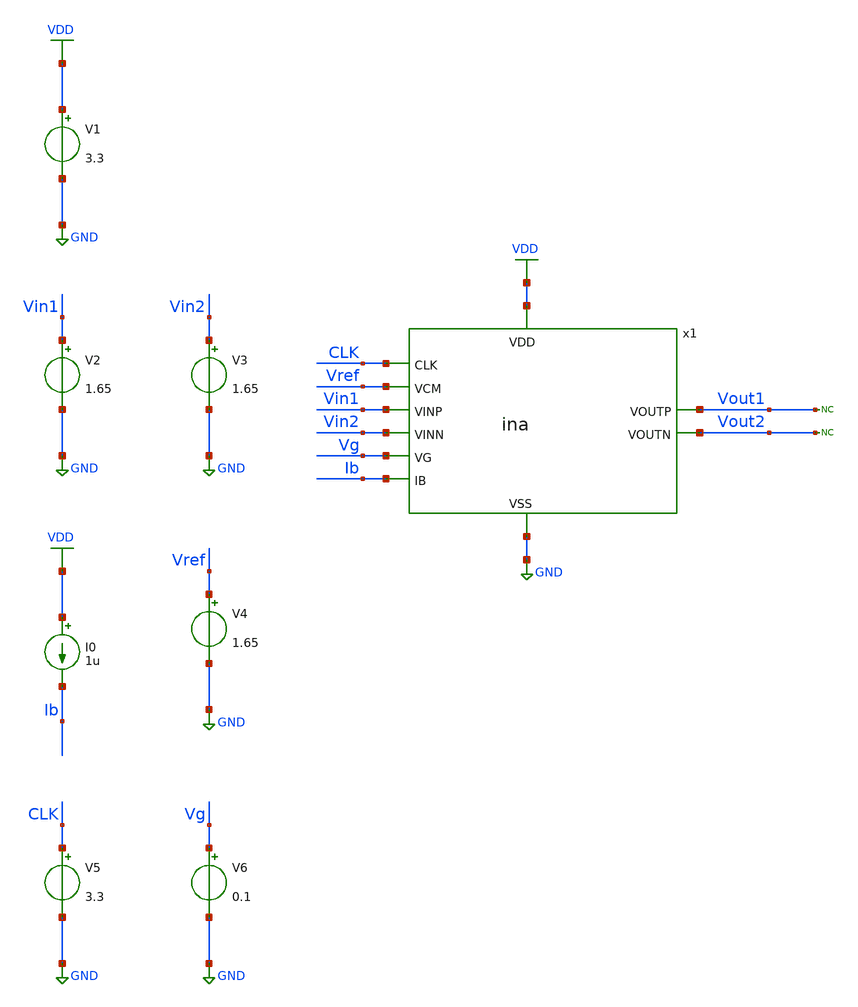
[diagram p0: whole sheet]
** sch_path: designs/libs/tb_ina/tb_ina_op/tb_ina_op.sch
**.subckt tb_ina_op
V1 VDD GND 3.3
V2 Vin1 GND 1.65
V3 Vin2 GND 1.65
V4 Vref GND 1.65
x1 Vg VDD Vin1 Vin2 CLK Vout1 Vout2 GND Vref Ib ina
V5 CLK GND 3.3
V6 Vg GND 0.1
I0 VDD Ib 1u
* noconn Vout1
* noconn Vout2
**** begin user architecture code

.include $::180MCU_MODELS/design.ngspice
.lib $::180MCU_MODELS/sm141064.ngspice typical
.lib $::180MCU_MODELS/sm141064.ngspice cap_mim
.lib $::180MCU_MODELS/sm141064.ngspice moscap_typical
.lib $::180MCU_MODELS/sm141064.ngspice mimcap_typical
.lib $::180MCU_MODELS/sm141064.ngspice res_typical
* .lib $::180MCU_MODELS/sm141064.ngspice res_statistical
* ngspice commands




.control
save all

set color0 = white

*************************************
** PARAMETERS
*************************************

let Vdd   = 3.3
let Vcm   = Vdd/2
let Vg    = 0.1
let Ibias = 2u

*************************************
** CHOPPER PARAMETERS
*************************************

let fchop = 4k
let tper = 1/fchop
let ton = tper/2
let tr = 10n
let tf = 10n

*************************************
** SOURCES
*************************************

alter @V1[DC] = $&Vdd
alter @V2[DC] = $&Vcm
alter @V3[DC] = $&Vcm
alter @V4[DC] = $&Vcm
alter @V5[PULSE] = [ 0 $&Vdd 0 $&tr $&tf $&ton $&tper 0 ]
alter @I0[DC] = $&Ibias
alter @V6[DC] = $&Vg

*************************************
** OPERATING POINT SIMULATION
*************************************

op

*************************************
** MEASUREMENTS
*************************************

let Idd = -i(V1)
let Pdis = $&Vdd*Idd

*************************************
** PRINT RESULTS
*************************************

display
show all
print Idd
print Pdis

*************************************
** SAVE
*************************************

write tb_ina_op.raw

.endc
* ngspice commands



**** end user architecture code
**.ends
.GLOBAL GND
.GLOBAL VDD
.end
